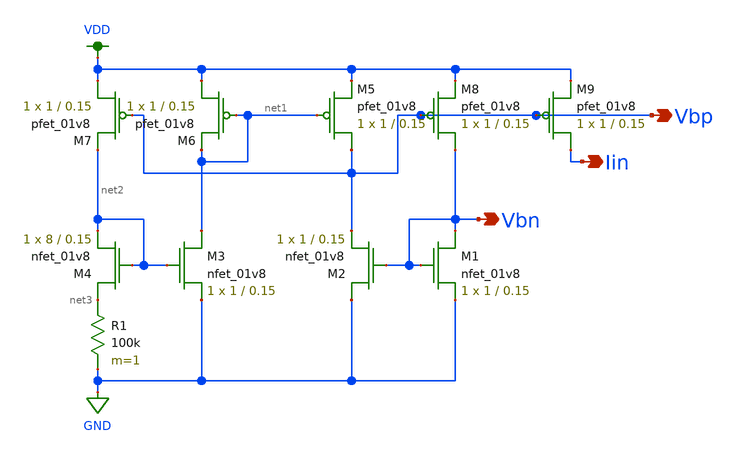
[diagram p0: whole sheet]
** sch_path: biasGen.sch
**.subckt biasGen Iin Vbp Vbn
*.opin Iin
*.opin Vbp
*.opin Vbn
XM1 Vbn Vbn GND GND sky130_fd_pr__nfet_01v8 L=0.15 W=1 nf=1 ad='int((nf+1)/2) * W/nf * 0.29' as='int((nf+2)/2) * W/nf * 0.29'
+ pd='2*int((nf+1)/2) * (W/nf + 0.29)' ps='2*int((nf+2)/2) * (W/nf + 0.29)' nrd='0.29 / W' nrs='0.29 / W'
+ sa=0 sb=0 sd=0 mult=1 m=1
XM2 GND Vbn Vbp GND sky130_fd_pr__nfet_01v8 L=0.15 W=1 nf=1 ad='int((nf+1)/2) * W/nf * 0.29' as='int((nf+2)/2) * W/nf * 0.29'
+ pd='2*int((nf+1)/2) * (W/nf + 0.29)' ps='2*int((nf+2)/2) * (W/nf + 0.29)' nrd='0.29 / W' nrs='0.29 / W'
+ sa=0 sb=0 sd=0 mult=1 m=1
XM3 net1 net2 GND GND sky130_fd_pr__nfet_01v8 L=0.15 W=1 nf=1 ad='int((nf+1)/2) * W/nf * 0.29' as='int((nf+2)/2) * W/nf * 0.29'
+ pd='2*int((nf+1)/2) * (W/nf + 0.29)' ps='2*int((nf+2)/2) * (W/nf + 0.29)' nrd='0.29 / W' nrs='0.29 / W'
+ sa=0 sb=0 sd=0 mult=1 m=1
XM4 net3 net2 net2 GND sky130_fd_pr__nfet_01v8 L=0.15 W=8 nf=1 ad='int((nf+1)/2) * W/nf * 0.29' as='int((nf+2)/2) * W/nf * 0.29'
+ pd='2*int((nf+1)/2) * (W/nf + 0.29)' ps='2*int((nf+2)/2) * (W/nf + 0.29)' nrd='0.29 / W' nrs='0.29 / W'
+ sa=0 sb=0 sd=0 mult=1 m=1
XM5 Vbp net1 VDD VDD sky130_fd_pr__pfet_01v8 L=0.15 W=1 nf=1 ad='int((nf+1)/2) * W/nf * 0.29' as='int((nf+2)/2) * W/nf * 0.29'
+ pd='2*int((nf+1)/2) * (W/nf + 0.29)' ps='2*int((nf+2)/2) * (W/nf + 0.29)' nrd='0.29 / W' nrs='0.29 / W'
+ sa=0 sb=0 sd=0 mult=1 m=1
XM6 VDD net1 net1 VDD sky130_fd_pr__pfet_01v8 L=0.15 W=1 nf=1 ad='int((nf+1)/2) * W/nf * 0.29' as='int((nf+2)/2) * W/nf * 0.29'
+ pd='2*int((nf+1)/2) * (W/nf + 0.29)' ps='2*int((nf+2)/2) * (W/nf + 0.29)' nrd='0.29 / W' nrs='0.29 / W'
+ sa=0 sb=0 sd=0 mult=1 m=1
XM7 VDD Vbp net2 VDD sky130_fd_pr__pfet_01v8 L=0.15 W=1 nf=1 ad='int((nf+1)/2) * W/nf * 0.29' as='int((nf+2)/2) * W/nf * 0.29'
+ pd='2*int((nf+1)/2) * (W/nf + 0.29)' ps='2*int((nf+2)/2) * (W/nf + 0.29)' nrd='0.29 / W' nrs='0.29 / W'
+ sa=0 sb=0 sd=0 mult=1 m=1
XM8 Vbn Vbp VDD VDD sky130_fd_pr__pfet_01v8 L=0.15 W=1 nf=1 ad='int((nf+1)/2) * W/nf * 0.29' as='int((nf+2)/2) * W/nf * 0.29'
+ pd='2*int((nf+1)/2) * (W/nf + 0.29)' ps='2*int((nf+2)/2) * (W/nf + 0.29)' nrd='0.29 / W' nrs='0.29 / W'
+ sa=0 sb=0 sd=0 mult=1 m=1
R1 net3 GND 100k m=1
XM9 Iin Vbp VDD VDD sky130_fd_pr__pfet_01v8 L=0.15 W=1 nf=1 ad='int((nf+1)/2) * W/nf * 0.29' as='int((nf+2)/2) * W/nf * 0.29'
+ pd='2*int((nf+1)/2) * (W/nf + 0.29)' ps='2*int((nf+2)/2) * (W/nf + 0.29)' nrd='0.29 / W' nrs='0.29 / W'
+ sa=0 sb=0 sd=0 mult=1 m=1
**.ends
.GLOBAL VDD
.GLOBAL GND
.end
